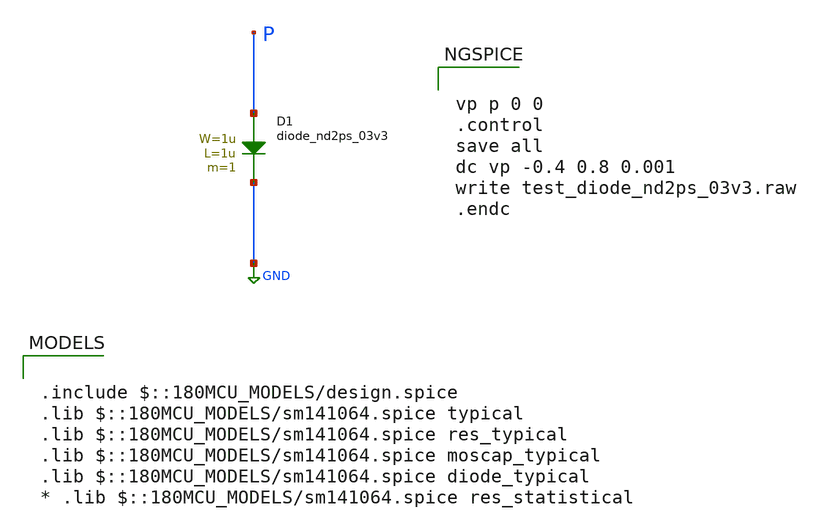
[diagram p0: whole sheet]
** sch_path: cells/xschem/tests/test_diode_nd2ps_03v3.sch
* Copyright 2022 GlobalFoundries PDK Authors
* Licensed under the Apache License, Version 2.0 (the "License");
* you may not use this file except in compliance with the License.
* You may obtain a copy of the License at
* https://www.apache.org/licenses/LICENSE-2.0
* Unless required by applicable law or agreed to in writing, software
* distributed under the License is distributed on an "AS IS" BASIS,
* WITHOUT WARRANTIES OR CONDITIONS OF ANY KIND, either express or implied.
* See the License for the specific language governing permissions and
* limitations under the License.
**.subckt test_diode_nd2ps_03v3
D1 P GND diode_nd2ps_03v3 area='1u * 1u ' pj='2*1u + 2*1u ' m=1
**** begin user architecture code

.include $::180MCU_MODELS/design.spice
.lib $::180MCU_MODELS/sm141064.spice typical
.lib $::180MCU_MODELS/sm141064.spice res_typical
.lib $::180MCU_MODELS/sm141064.spice moscap_typical
.lib $::180MCU_MODELS/sm141064.spice diode_typical
* .lib $::180MCU_MODELS/sm141064.spice res_statistical



vp p 0 0
.control
save all
dc vp -0.4 0.8 0.001
write test_diode_nd2ps_03v3.raw
.endc


**** end user architecture code
**.ends
.GLOBAL GND
.end
